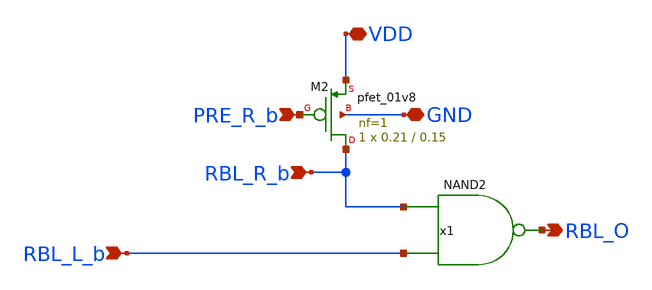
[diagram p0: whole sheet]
** sch_path: custom/xschem/local_eval.sch
**.subckt local_eval PRE_R_b RBL_L_b RBL_R_b RBL_O VDD GND
*.ipin PRE_R_b
*.ipin RBL_L_b
*.ipin RBL_R_b
*.opin RBL_O
*.iopin VDD
*.iopin GND
XM2 RBL_R_b PRE_R_b VDD GND sky130_fd_pr__pfet_01v8 L=0.15 W=0.21 nf=1 ad='int((nf+1)/2) * W/nf * 0.29'
+ as='int((nf+2)/2) * W/nf * 0.29' pd='2*int((nf+1)/2) * (W/nf + 0.29)' ps='2*int((nf+2)/2) * (W/nf + 0.29)'
+ nrd='0.29 / W' nrs='0.29 / W' sa=0 sb=0 sd=0 mult=1 m=1
x1 RBL_O RBL_R_b RBL_L_b VCC VSS VCC VSS NAND2
**.ends
.end
